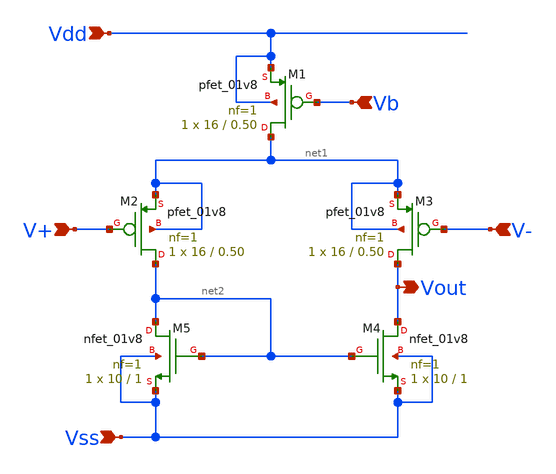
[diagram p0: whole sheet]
** sch_path: Bandgap/ota.sch
**.subckt ota Vdd Vout V+ V- Vss Vb
*.ipin Vdd
*.opin Vout
*.ipin V+
*.ipin V-
*.ipin Vss
*.ipin Vb
XM1 net1 Vb Vdd Vdd sky130_fd_pr__pfet_01v8 L=0.50 W=16 nf=1 ad='int((1 + 1)/2) * 16 / 1 * 0.29' as='int((1 + 2)/2) * 16 / 1 * 0.29'
+ pd='2*int((1 + 1)/2) * (16 / 1 + 0.29)' ps='2*int((1 + 2)/2) * (16 / 1 + 0.29)' nrd='0.29 / 16 ' nrs='0.29 / 16 '
+ sa=0 sb=0 sd=0 mult=1 m=1
XM2 net2 V+ net1 net1 sky130_fd_pr__pfet_01v8 L=0.50 W=16 nf=1 ad='int((1 + 1)/2) * 16 / 1 * 0.29' as='int((1 + 2)/2) * 16 / 1 * 0.29'
+ pd='2*int((1 + 1)/2) * (16 / 1 + 0.29)' ps='2*int((1 + 2)/2) * (16 / 1 + 0.29)' nrd='0.29 / 16 ' nrs='0.29 / 16 '
+ sa=0 sb=0 sd=0 mult=1 m=1
XM3 Vout V- net1 net1 sky130_fd_pr__pfet_01v8 L=0.50 W=16 nf=1 ad='int((1 + 1)/2) * 16 / 1 * 0.29' as='int((1 + 2)/2) * 16 / 1 * 0.29'
+ pd='2*int((1 + 1)/2) * (16 / 1 + 0.29)' ps='2*int((1 + 2)/2) * (16 / 1 + 0.29)' nrd='0.29 / 16 ' nrs='0.29 / 16 '
+ sa=0 sb=0 sd=0 mult=1 m=1
XM4 Vout net2 Vss Vss sky130_fd_pr__nfet_01v8 L=1 W=10 nf=1 ad='int((1 + 1)/2) * 10 / 1 * 0.29' as='int((1 + 2)/2) * 10 / 1 * 0.29'
+ pd='2*int((1 + 1)/2) * (10 / 1 + 0.29)' ps='2*int((1 + 2)/2) * (10 / 1 + 0.29)' nrd='0.29 / 10 ' nrs='0.29 / 10 '
+ sa=0 sb=0 sd=0 mult=1 m=1
XM5 net2 net2 Vss Vss sky130_fd_pr__nfet_01v8 L=1 W=10 nf=1 ad='int((1 + 1)/2) * 10 / 1 * 0.29' as='int((1 + 2)/2) * 10 / 1 * 0.29'
+ pd='2*int((1 + 1)/2) * (10 / 1 + 0.29)' ps='2*int((1 + 2)/2) * (10 / 1 + 0.29)' nrd='0.29 / 10 ' nrs='0.29 / 10 '
+ sa=0 sb=0 sd=0 mult=1 m=1
**.ends
.end
